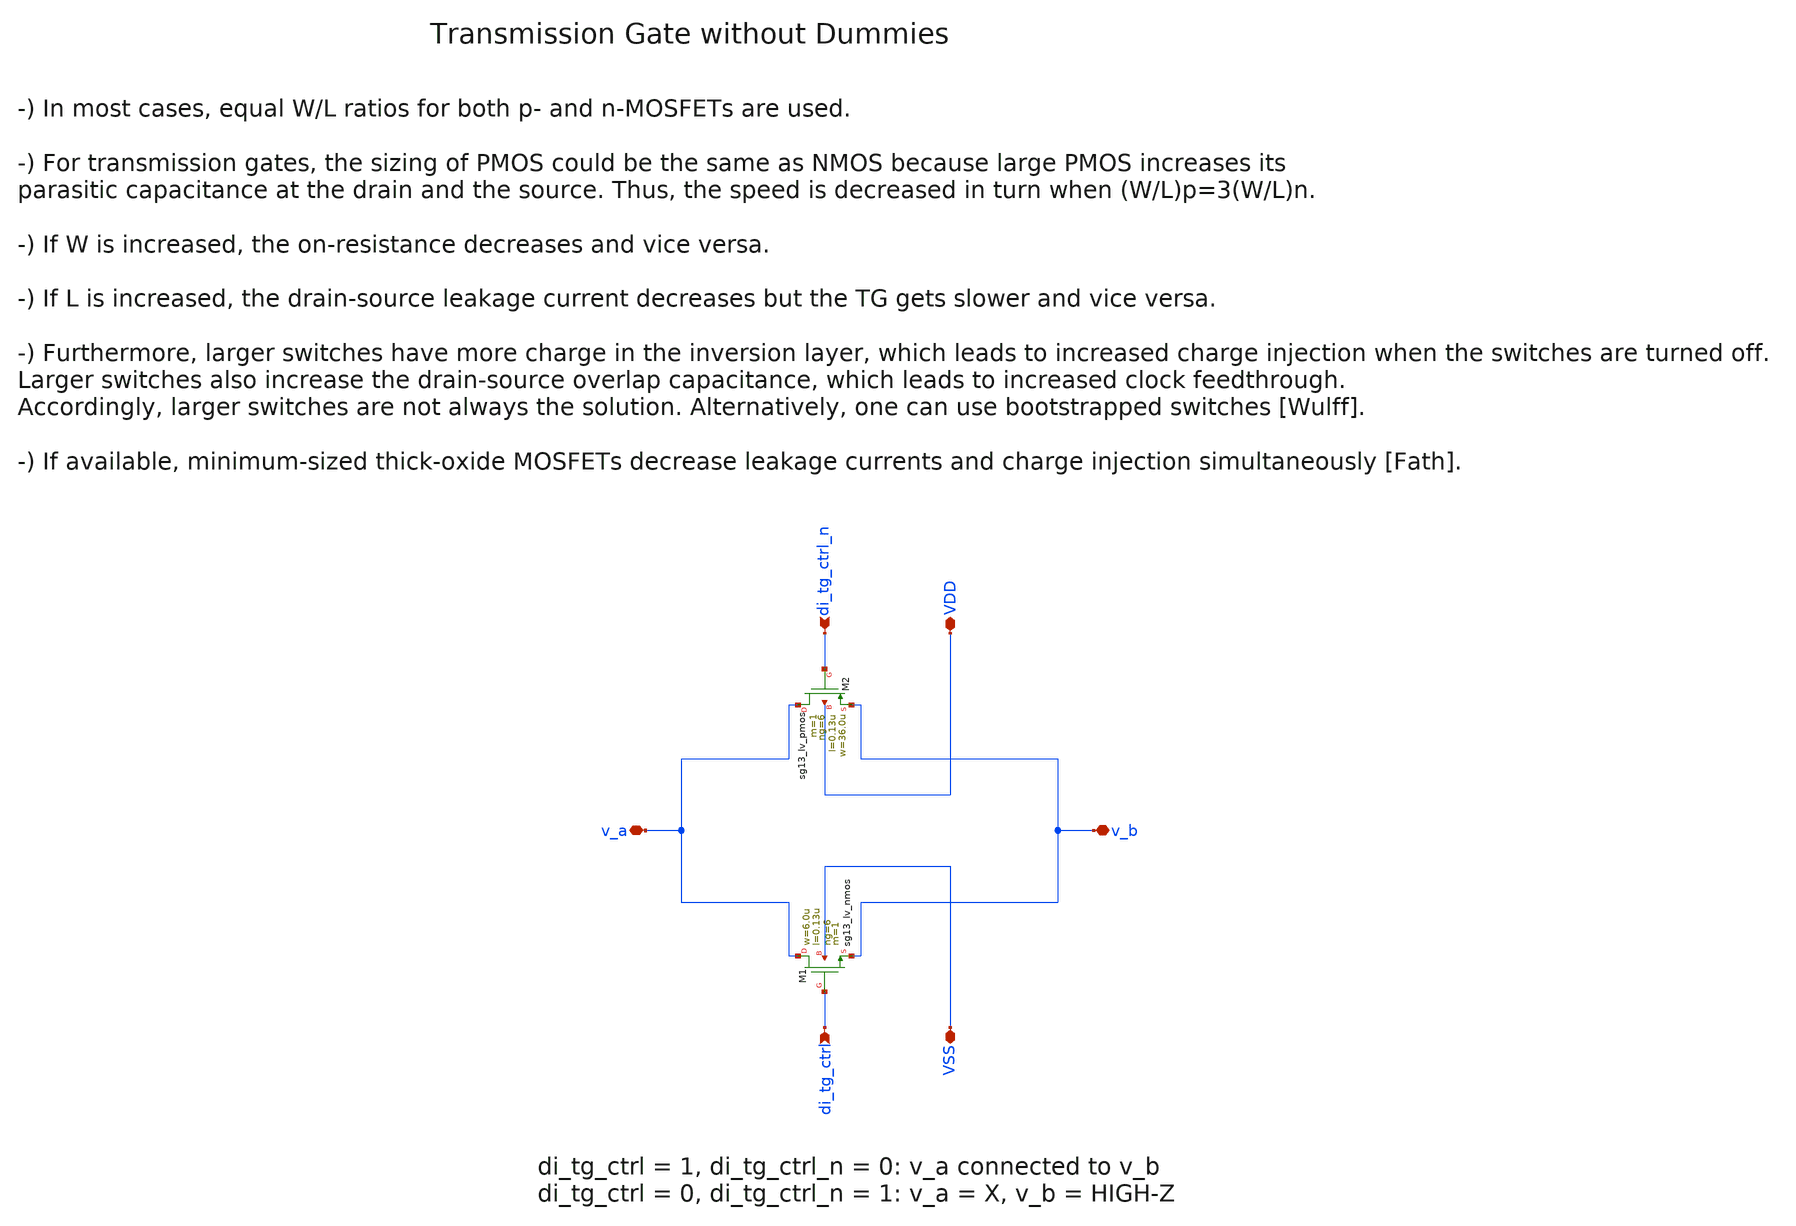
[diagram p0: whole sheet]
** sch_path: ihp130/macros/iqmod/schematic/iqmod_mfb_lpf_ota_core_tg.sch
**.subckt iqmod_mfb_lpf_ota_core_tg v_a v_b VDD VSS di_tg_ctrl di_tg_ctrl_n
*.iopin v_a
*.iopin v_b
*.iopin VDD
*.iopin VSS
*.ipin di_tg_ctrl
*.ipin di_tg_ctrl_n
XM2 v_a di_tg_ctrl_n v_b VDD sg13_lv_pmos w=36.0u l=0.13u ng=6 m=1 mm_ok=1
XM1 v_a di_tg_ctrl v_b VSS sg13_lv_nmos w=6.0u l=0.13u ng=6 m=1 mm_ok=1
**.ends
.end
